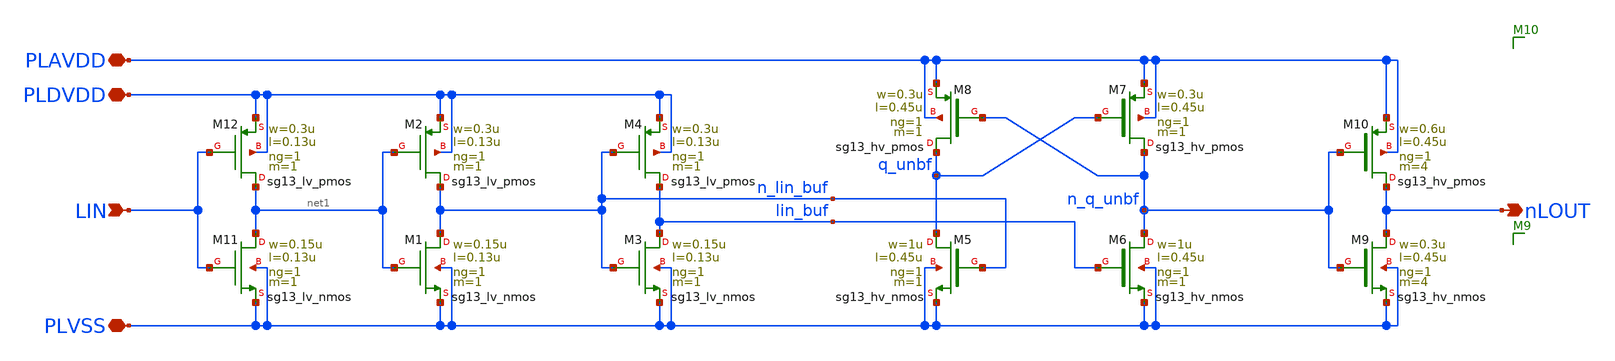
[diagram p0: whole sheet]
** sch_path: xschem/inverting_digital_level_translator.sch
**.subckt inverting_digital_level_translator PLAVDD PLVSS PLDVDD LIN nLOUT
*.iopin PLAVDD
*.iopin PLVSS
*.iopin PLDVDD
*.ipin LIN
*.opin nLOUT
XM1 n_lin_buf net1 PLVSS PLVSS sg13_lv_nmos w=0.15u l=0.13u ng=1 m=1 mm_ok=1
XM2 n_lin_buf net1 PLDVDD PLDVDD sg13_lv_pmos w=0.3u l=0.13u ng=1 m=1 mm_ok=1
XM3 lin_buf n_lin_buf PLVSS PLVSS sg13_lv_nmos w=0.15u l=0.13u ng=1 m=1 mm_ok=1
XM4 lin_buf n_lin_buf PLDVDD PLDVDD sg13_lv_pmos w=0.3u l=0.13u ng=1 m=1 mm_ok=1
XM5 q_unbf n_lin_buf PLVSS PLVSS sg13_hv_nmos w=1u l=0.45u ng=1 m=1 mm_ok=1
XM6 n_q_unbf lin_buf PLVSS PLVSS sg13_hv_nmos w=1u l=0.45u ng=1 m=1 mm_ok=1
XM7 n_q_unbf q_unbf PLAVDD PLAVDD sg13_hv_pmos w=0.3u l=0.45u ng=1 m=1 mm_ok=1
XM9 nLOUT n_q_unbf PLVSS PLVSS sg13_hv_nmos w=0.3u l=0.45u ng=1 m=4 mm_ok=1
XM10 nLOUT n_q_unbf PLAVDD PLAVDD sg13_hv_pmos w=0.6u l=0.45u ng=1 m=4 mm_ok=1
XM8 q_unbf n_q_unbf PLAVDD PLAVDD sg13_hv_pmos w=0.3u l=0.45u ng=1 m=1 mm_ok=1
XM11 net1 LIN PLVSS PLVSS sg13_lv_nmos w=0.15u l=0.13u ng=1 m=1 mm_ok=1
XM12 net1 LIN PLDVDD PLDVDD sg13_lv_pmos w=0.3u l=0.13u ng=1 m=1 mm_ok=1
**.ends
.end
